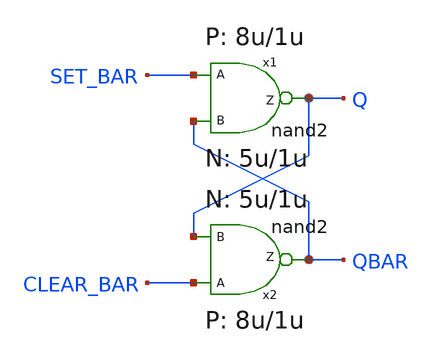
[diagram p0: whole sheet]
** sch_path: examples/xschem_examples/test.sch
* Copyright (C) 1998-2023 Stefan Frederik Schippers
* This program is free software; you can redistribute it and/or modify
* it under the terms of the GNU General Public License as published by
* the Free Software Foundation; either version 2 of the License, or
* (at your option) any later version.
* This program is distributed in the hope that it will be useful,
* but WITHOUT ANY WARRANTY; without even the implied warranty of
* MERCHANTABILITY or FITNESS FOR A PARTICULAR PURPOSE.  See the
* GNU General Public License for more details.
* You should have received a copy of the GNU General Public License
* along with this program; if not, write to the Free Software
**.subckt test
x1 Q SET_BAR QBAR nand2 WP=8u LP=1u WN=5u LLN=1u
x2 QBAR CLEAR_BAR Q nand2 WP=8u LP=1u WN=5u LLN=1u
**.ends

* expanding   symbol:  nand2.sym # of pins=3
** sym_path: examples/xschem_examples/nand2.sym
** sch_path: examples/xschem_examples/nand2.sch
.subckt nand2 Z A B  WP=8u LP=1u WN=5u LLN=1u
*.ipin A
*.opin Z
*.ipin B
m1 Z A net1 VSS CMOSN w=WN l=LLN m=1
m1 net1 B VSS VSS CMOSN w=WN l=LLN m=1
m2 Z B VCC VCC CMOSP w=WP l=LP m=1
m2 Z A VCC VCC CMOSP w=WP l=LP m=1
.ends

.GLOBAL VSS
.GLOBAL VCC
.end
